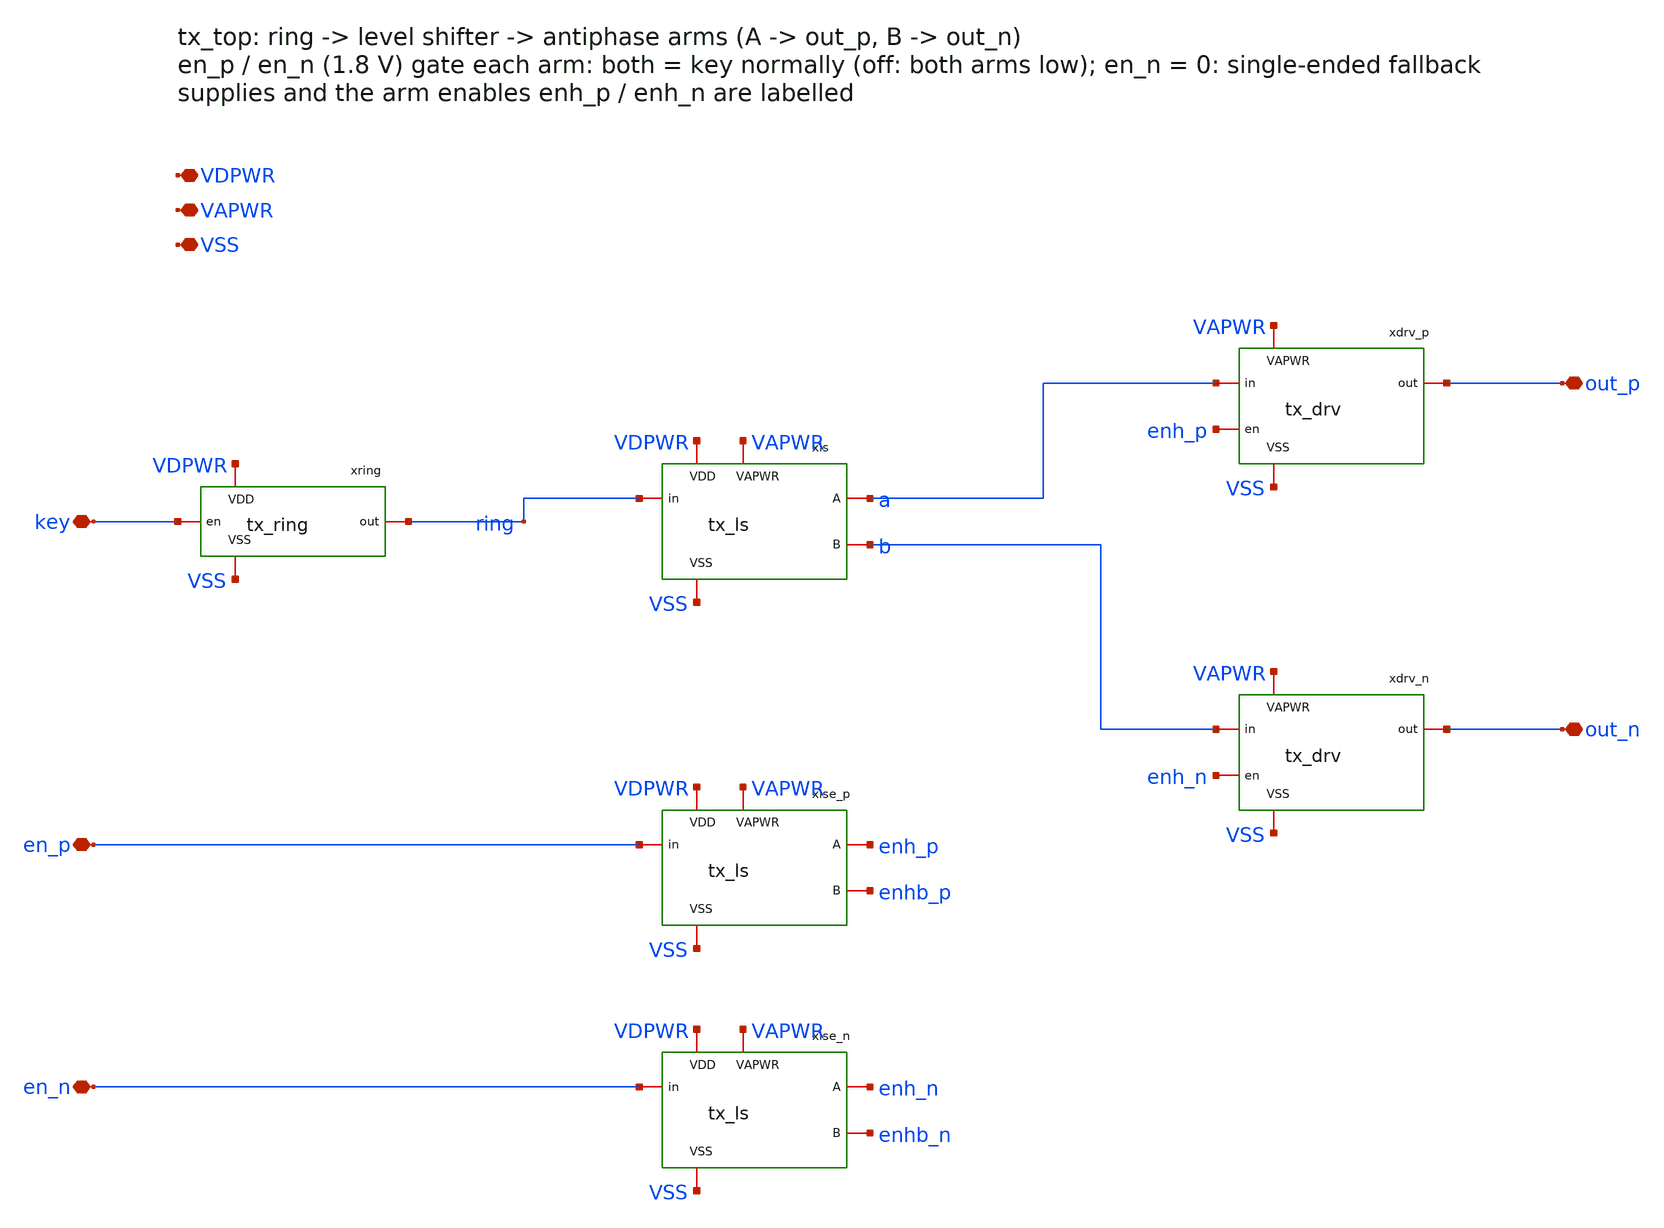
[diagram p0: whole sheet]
** sch_path: xschem/tx_top.sch
**.subckt tx_top VDPWR VAPWR VSS key en_p en_n out_p out_n
*.iopin VDPWR
*.iopin VAPWR
*.iopin VSS
*.iopin key
*.iopin en_p
*.iopin en_n
*.iopin out_p
*.iopin out_n
xring key ring VDPWR VSS tx_ring cw=3.2f
xls ring a b VDPWR VAPWR VSS tx_ls kn=14 kp=8 wpi=9 wni=3
xlse_p en_p enh_p enhb_p VDPWR VAPWR VSS tx_ls kn=1 kp=1 wpi=1 wni=0.42
xdrv_p a enh_p out_p VAPWR VSS tx_drv
xlse_n en_n enh_n enhb_n VDPWR VAPWR VSS tx_ls kn=1 kp=1 wpi=1 wni=0.42
xdrv_n b enh_n out_n VAPWR VSS tx_drv
**.ends

* expanding   symbol:  tx_ring.sym # of pins=4
** sym_path: xschem/tx_ring.sym
** sch_path: xschem/tx_ring.sch
.subckt tx_ring en out VDD VSS  cw=3.2f
*.iopin VDD
*.iopin VSS
*.iopin en
*.iopin out
xr0 en r22 VSS VSS VDD VDD out sky130_fd_sc_hd__nand2_2
Cr0 out VSS 'cw' m=1
xr1 out VSS VSS VDD VDD r1 sky130_fd_sc_hd__inv_2
Cr1 r1 VSS 'cw' m=1
xr2 r1 VSS VSS VDD VDD r2 sky130_fd_sc_hd__inv_2
Cr2 r2 VSS 'cw' m=1
xr3 r2 VSS VSS VDD VDD r3 sky130_fd_sc_hd__inv_2
Cr3 r3 VSS 'cw' m=1
xr4 r3 VSS VSS VDD VDD r4 sky130_fd_sc_hd__inv_2
Cr4 r4 VSS 'cw' m=1
xr5 r4 VSS VSS VDD VDD r5 sky130_fd_sc_hd__inv_2
Cr5 r5 VSS 'cw' m=1
xr6 r5 VSS VSS VDD VDD r6 sky130_fd_sc_hd__inv_2
Cr6 r6 VSS 'cw' m=1
xr7 r6 VSS VSS VDD VDD r7 sky130_fd_sc_hd__inv_2
Cr7 r7 VSS 'cw' m=1
xr8 r7 VSS VSS VDD VDD r8 sky130_fd_sc_hd__inv_2
Cr8 r8 VSS 'cw' m=1
xr9 r8 VSS VSS VDD VDD r9 sky130_fd_sc_hd__inv_2
Cr9 r9 VSS 'cw' m=1
xr10 r9 VSS VSS VDD VDD r10 sky130_fd_sc_hd__inv_2
Cr10 r10 VSS 'cw' m=1
xr11 r10 VSS VSS VDD VDD r11 sky130_fd_sc_hd__inv_2
Cr11 r11 VSS 'cw' m=1
xr12 r11 VSS VSS VDD VDD r12 sky130_fd_sc_hd__inv_2
Cr12 r12 VSS 'cw' m=1
xr13 r12 VSS VSS VDD VDD r13 sky130_fd_sc_hd__inv_2
Cr13 r13 VSS 'cw' m=1
xr14 r13 VSS VSS VDD VDD r14 sky130_fd_sc_hd__inv_2
Cr14 r14 VSS 'cw' m=1
xr15 r14 VSS VSS VDD VDD r15 sky130_fd_sc_hd__inv_2
Cr15 r15 VSS 'cw' m=1
xr16 r15 VSS VSS VDD VDD r16 sky130_fd_sc_hd__inv_2
Cr16 r16 VSS 'cw' m=1
xr17 r16 VSS VSS VDD VDD r17 sky130_fd_sc_hd__inv_2
Cr17 r17 VSS 'cw' m=1
xr18 r17 VSS VSS VDD VDD r18 sky130_fd_sc_hd__inv_2
Cr18 r18 VSS 'cw' m=1
xr19 r18 VSS VSS VDD VDD r19 sky130_fd_sc_hd__inv_2
Cr19 r19 VSS 'cw' m=1
xr20 r19 VSS VSS VDD VDD r20 sky130_fd_sc_hd__inv_2
Cr20 r20 VSS 'cw' m=1
xr21 r20 VSS VSS VDD VDD r21 sky130_fd_sc_hd__inv_2
Cr21 r21 VSS 'cw' m=1
xr22 r21 VSS VSS VDD VDD r22 sky130_fd_sc_hd__inv_2
Cr22 r22 VSS 'cw' m=1
.ends


* expanding   symbol:  tx_ls.sym # of pins=6
** sym_path: xschem/tx_ls.sym
** sch_path: xschem/tx_ls.sch
.subckt tx_ls in A B VDD VAPWR VSS  kn=14 kp=8 wpi=9 wni=3
*.iopin VDD
*.iopin VAPWR
*.iopin VSS
*.iopin in
*.iopin A
*.iopin B
XMi1p ctrl in VDD VDD sky130_fd_pr__pfet_01v8 L=0.15 W='wpi' nf=1 ad='int((nf+1)/2) * W/nf * 0.29' as='int((nf+2)/2) * W/nf * 0.29'
+ pd='2*int((nf+1)/2) * (W/nf + 0.29)' ps='2*int((nf+2)/2) * (W/nf + 0.29)' nrd='0.29 / W' nrs='0.29 / W'
+ sa=0 sb=0 sd=0 mult=1 m=1
XMi1n ctrl in VSS VSS sky130_fd_pr__nfet_01v8 L=0.15 W='wni' nf=1 ad='int((nf+1)/2) * W/nf * 0.29' as='int((nf+2)/2) * W/nf * 0.29'
+ pd='2*int((nf+1)/2) * (W/nf + 0.29)' ps='2*int((nf+2)/2) * (W/nf + 0.29)' nrd='0.29 / W' nrs='0.29 / W'
+ sa=0 sb=0 sd=0 mult=1 m=1
XM8 ctrl_n ctrl VDD VDD sky130_fd_pr__pfet_01v8_hvt L=0.15 W=4 nf=1 ad='int((nf+1)/2) * W/nf * 0.29'
+ as='int((nf+2)/2) * W/nf * 0.29' pd='2*int((nf+1)/2) * (W/nf + 0.29)' ps='2*int((nf+2)/2) * (W/nf + 0.29)'
+ nrd='0.29 / W' nrs='0.29 / W' sa=0 sb=0 sd=0 mult=1 m=1
XM7 ctrl_n ctrl VSS VSS sky130_fd_pr__nfet_01v8 L=0.15 W=1.68 nf=1 ad='int((nf+1)/2) * W/nf * 0.29' as='int((nf+2)/2) * W/nf * 0.29'
+ pd='2*int((nf+1)/2) * (W/nf + 0.29)' ps='2*int((nf+2)/2) * (W/nf + 0.29)' nrd='0.29 / W' nrs='0.29 / W'
+ sa=0 sb=0 sd=0 mult=1 m=1
XM9 A ctrl VSS VSS sky130_fd_pr__nfet_g5v0d10v5 L=0.5 W='0.42*kn' nf=1 ad='int((nf+1)/2) * W/nf * 0.29'
+ as='int((nf+2)/2) * W/nf * 0.29' pd='2*int((nf+1)/2) * (W/nf + 0.29)' ps='2*int((nf+2)/2) * (W/nf + 0.29)'
+ nrd='0.29 / W' nrs='0.29 / W' sa=0 sb=0 sd=0 mult=1 m=1
XM10 B ctrl_n VSS VSS sky130_fd_pr__nfet_g5v0d10v5 L=0.5 W='0.42*kn' nf=1 ad='int((nf+1)/2) * W/nf * 0.29'
+ as='int((nf+2)/2) * W/nf * 0.29' pd='2*int((nf+1)/2) * (W/nf + 0.29)' ps='2*int((nf+2)/2) * (W/nf + 0.29)'
+ nrd='0.29 / W' nrs='0.29 / W' sa=0 sb=0 sd=0 mult=1 m=1
XM11 A B VAPWR VAPWR sky130_fd_pr__pfet_g5v0d10v5 L=0.5 W='0.42*kp' nf=1 ad='int((nf+1)/2) * W/nf * 0.29'
+ as='int((nf+2)/2) * W/nf * 0.29' pd='2*int((nf+1)/2) * (W/nf + 0.29)' ps='2*int((nf+2)/2) * (W/nf + 0.29)'
+ nrd='0.29 / W' nrs='0.29 / W' sa=0 sb=0 sd=0 mult=1 m=1
XM12 B A VAPWR VAPWR sky130_fd_pr__pfet_g5v0d10v5 L=0.5 W='0.42*kp' nf=1 ad='int((nf+1)/2) * W/nf * 0.29'
+ as='int((nf+2)/2) * W/nf * 0.29' pd='2*int((nf+1)/2) * (W/nf + 0.29)' ps='2*int((nf+2)/2) * (W/nf + 0.29)'
+ nrd='0.29 / W' nrs='0.29 / W' sa=0 sb=0 sd=0 mult=1 m=1
.ends


* expanding   symbol:  tx_drv.sym # of pins=5
** sym_path: xschem/tx_drv.sym
** sch_path: xschem/tx_drv.sch
.subckt tx_drv in en out VAPWR VSS
*.iopin VAPWR
*.iopin VSS
*.iopin in
*.iopin en
*.iopin out
XMnap y0 in VAPWR VAPWR sky130_fd_pr__pfet_g5v0d10v5 L=0.5 W=1.26 nf=1 ad='int((nf+1)/2) * W/nf * 0.29'
+ as='int((nf+2)/2) * W/nf * 0.29' pd='2*int((nf+1)/2) * (W/nf + 0.29)' ps='2*int((nf+2)/2) * (W/nf + 0.29)'
+ nrd='0.29 / W' nrs='0.29 / W' sa=0 sb=0 sd=0 mult=1 m=1
XMnbp y0 en VAPWR VAPWR sky130_fd_pr__pfet_g5v0d10v5 L=0.5 W=1.26 nf=1 ad='int((nf+1)/2) * W/nf * 0.29'
+ as='int((nf+2)/2) * W/nf * 0.29' pd='2*int((nf+1)/2) * (W/nf + 0.29)' ps='2*int((nf+2)/2) * (W/nf + 0.29)'
+ nrd='0.29 / W' nrs='0.29 / W' sa=0 sb=0 sd=0 mult=1 m=1
XMnan y0 in ns VSS sky130_fd_pr__nfet_g5v0d10v5 L=0.5 W=0.84 nf=1 ad='int((nf+1)/2) * W/nf * 0.29' as='int((nf+2)/2) * W/nf * 0.29'
+ pd='2*int((nf+1)/2) * (W/nf + 0.29)' ps='2*int((nf+2)/2) * (W/nf + 0.29)' nrd='0.29 / W' nrs='0.29 / W'
+ sa=0 sb=0 sd=0 mult=1 m=1
XMnbn ns en VSS VSS sky130_fd_pr__nfet_g5v0d10v5 L=0.5 W=0.84 nf=1 ad='int((nf+1)/2) * W/nf * 0.29' as='int((nf+2)/2) * W/nf * 0.29'
+ pd='2*int((nf+1)/2) * (W/nf + 0.29)' ps='2*int((nf+2)/2) * (W/nf + 0.29)' nrd='0.29 / W' nrs='0.29 / W'
+ sa=0 sb=0 sd=0 mult=1 m=1
XM1p y1 y0 VAPWR VAPWR sky130_fd_pr__pfet_g5v0d10v5 L=0.5 W=1.26 nf=1 ad='int((nf+1)/2) * W/nf * 0.29'
+ as='int((nf+2)/2) * W/nf * 0.29' pd='2*int((nf+1)/2) * (W/nf + 0.29)' ps='2*int((nf+2)/2) * (W/nf + 0.29)'
+ nrd='0.29 / W' nrs='0.29 / W' sa=0 sb=0 sd=0 mult=1 m=1
XM1n y1 y0 VSS VSS sky130_fd_pr__nfet_g5v0d10v5 L=0.5 W=0.42 nf=1 ad='int((nf+1)/2) * W/nf * 0.29' as='int((nf+2)/2) * W/nf * 0.29'
+ pd='2*int((nf+1)/2) * (W/nf + 0.29)' ps='2*int((nf+2)/2) * (W/nf + 0.29)' nrd='0.29 / W' nrs='0.29 / W'
+ sa=0 sb=0 sd=0 mult=1 m=1
XM2p y2 y1 VAPWR VAPWR sky130_fd_pr__pfet_g5v0d10v5 L=0.5 W=5.04 nf=1 ad='int((nf+1)/2) * W/nf * 0.29'
+ as='int((nf+2)/2) * W/nf * 0.29' pd='2*int((nf+1)/2) * (W/nf + 0.29)' ps='2*int((nf+2)/2) * (W/nf + 0.29)'
+ nrd='0.29 / W' nrs='0.29 / W' sa=0 sb=0 sd=0 mult=1 m=1
XM2n y2 y1 VSS VSS sky130_fd_pr__nfet_g5v0d10v5 L=0.5 W=1.68 nf=1 ad='int((nf+1)/2) * W/nf * 0.29' as='int((nf+2)/2) * W/nf * 0.29'
+ pd='2*int((nf+1)/2) * (W/nf + 0.29)' ps='2*int((nf+2)/2) * (W/nf + 0.29)' nrd='0.29 / W' nrs='0.29 / W'
+ sa=0 sb=0 sd=0 mult=1 m=1
XM3p y3 y2 VAPWR VAPWR sky130_fd_pr__pfet_g5v0d10v5 L=0.5 W=20.16 nf=2 ad='int((nf+1)/2) * W/nf * 0.29'
+ as='int((nf+2)/2) * W/nf * 0.29' pd='2*int((nf+1)/2) * (W/nf + 0.29)' ps='2*int((nf+2)/2) * (W/nf + 0.29)'
+ nrd='0.29 / W' nrs='0.29 / W' sa=0 sb=0 sd=0 mult=1 m=1
XM3n y3 y2 VSS VSS sky130_fd_pr__nfet_g5v0d10v5 L=0.5 W=6.72 nf=1 ad='int((nf+1)/2) * W/nf * 0.29' as='int((nf+2)/2) * W/nf * 0.29'
+ pd='2*int((nf+1)/2) * (W/nf + 0.29)' ps='2*int((nf+2)/2) * (W/nf + 0.29)' nrd='0.29 / W' nrs='0.29 / W'
+ sa=0 sb=0 sd=0 mult=1 m=1
XM4p y4 y3 VAPWR VAPWR sky130_fd_pr__pfet_g5v0d10v5 L=0.5 W=80.64 nf=8 ad='int((nf+1)/2) * W/nf * 0.29'
+ as='int((nf+2)/2) * W/nf * 0.29' pd='2*int((nf+1)/2) * (W/nf + 0.29)' ps='2*int((nf+2)/2) * (W/nf + 0.29)'
+ nrd='0.29 / W' nrs='0.29 / W' sa=0 sb=0 sd=0 mult=1 m=1
XM4n y4 y3 VSS VSS sky130_fd_pr__nfet_g5v0d10v5 L=0.5 W=26.88 nf=3 ad='int((nf+1)/2) * W/nf * 0.29' as='int((nf+2)/2) * W/nf * 0.29'
+ pd='2*int((nf+1)/2) * (W/nf + 0.29)' ps='2*int((nf+2)/2) * (W/nf + 0.29)' nrd='0.29 / W' nrs='0.29 / W'
+ sa=0 sb=0 sd=0 mult=1 m=1
XM5p out y4 VAPWR VAPWR sky130_fd_pr__pfet_g5v0d10v5 L=0.5 W=144 nf=14 ad='int((nf+1)/2) * W/nf * 0.29'
+ as='int((nf+2)/2) * W/nf * 0.29' pd='2*int((nf+1)/2) * (W/nf + 0.29)' ps='2*int((nf+2)/2) * (W/nf + 0.29)'
+ nrd='0.29 / W' nrs='0.29 / W' sa=0 sb=0 sd=0 mult=1 m=1
XM5n out y4 VSS VSS sky130_fd_pr__nfet_g5v0d10v5 L=0.5 W=48 nf=5 ad='int((nf+1)/2) * W/nf * 0.29' as='int((nf+2)/2) * W/nf * 0.29'
+ pd='2*int((nf+1)/2) * (W/nf + 0.29)' ps='2*int((nf+2)/2) * (W/nf + 0.29)' nrd='0.29 / W' nrs='0.29 / W'
+ sa=0 sb=0 sd=0 mult=1 m=1
.ends

.end
